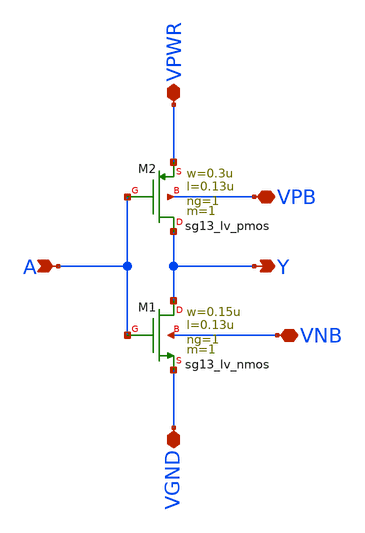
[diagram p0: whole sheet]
** sch_path: Team 2 Design/design_data/xschem/t2_vco_inverter.sch
**.subckt t2_vco_inverter VPWR VGND A Y VPB VNB
*.iopin VPWR
*.iopin VGND
*.ipin A
*.opin Y
*.iopin VPB
*.iopin VNB
XM2 Y A VPWR VPB sg13_lv_pmos w=0.3u l=0.13u ng=1 m=1 mm_ok=1
XM1 Y A VGND VNB sg13_lv_nmos w=0.15u l=0.13u ng=1 m=1 mm_ok=1
**.ends
.end
